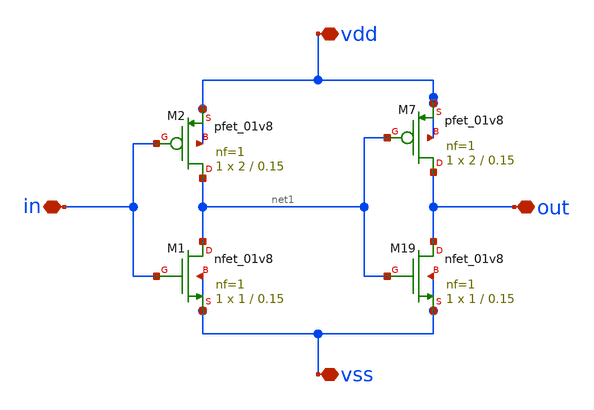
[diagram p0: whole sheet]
** sch_path: untitled-1.sch
**.subckt untitled-1 out in vss vdd
*.iopin out
*.iopin in
*.iopin vss
*.iopin vdd
XM19 out net1 vss vss sky130_fd_pr__nfet_01v8 L=0.15 W=1 nf=1 ad='int((nf+1)/2) * W/nf * 0.29' as='int((nf+2)/2) * W/nf * 0.29'
+ pd='2*int((nf+1)/2) * (W/nf + 0.29)' ps='2*int((nf+2)/2) * (W/nf + 0.29)' nrd='0.29 / W' nrs='0.29 / W'
+ sa=0 sb=0 sd=0 mult=1 m=1
XM1 net1 in vss vss sky130_fd_pr__nfet_01v8 L=0.15 W=1 nf=1 ad='int((nf+1)/2) * W/nf * 0.29' as='int((nf+2)/2) * W/nf * 0.29'
+ pd='2*int((nf+1)/2) * (W/nf + 0.29)' ps='2*int((nf+2)/2) * (W/nf + 0.29)' nrd='0.29 / W' nrs='0.29 / W'
+ sa=0 sb=0 sd=0 mult=1 m=1
XM7 out net1 vdd vdd sky130_fd_pr__pfet_01v8 L=0.15 W=2 nf=1 ad='int((nf+1)/2) * W/nf * 0.29' as='int((nf+2)/2) * W/nf * 0.29'
+ pd='2*int((nf+1)/2) * (W/nf + 0.29)' ps='2*int((nf+2)/2) * (W/nf + 0.29)' nrd='0.29 / W' nrs='0.29 / W'
+ sa=0 sb=0 sd=0 mult=1 m=1
XM2 net1 in vdd vdd sky130_fd_pr__pfet_01v8 L=0.15 W=2 nf=1 ad='int((nf+1)/2) * W/nf * 0.29' as='int((nf+2)/2) * W/nf * 0.29'
+ pd='2*int((nf+1)/2) * (W/nf + 0.29)' ps='2*int((nf+2)/2) * (W/nf + 0.29)' nrd='0.29 / W' nrs='0.29 / W'
+ sa=0 sb=0 sd=0 mult=1 m=1
**.ends
.end
